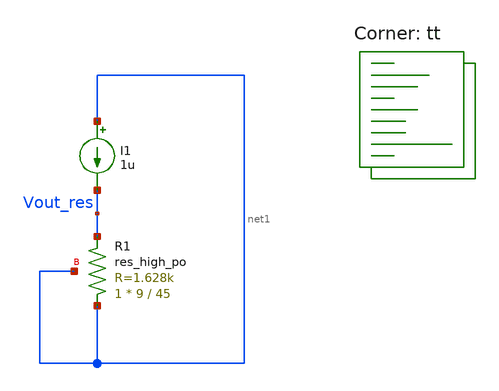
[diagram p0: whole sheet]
** sch_path: xschem/misc/testing/res_xhigh.sch
**.subckt res_xhigh
I1 net1 Vout_res 1u
XR1 net1 Vout_res net1 sky130_fd_pr__res_high_po W=9 L=45 mult=1 m=1
**** begin user architecture code
.lib $::SKYWATER_MODELS/sky130.lib.spice tt


.param temp=27

.dc temp -25 100 1


.save all
.control
run
plot Vout_res
.endc



**** end user architecture code
**.ends
.end
